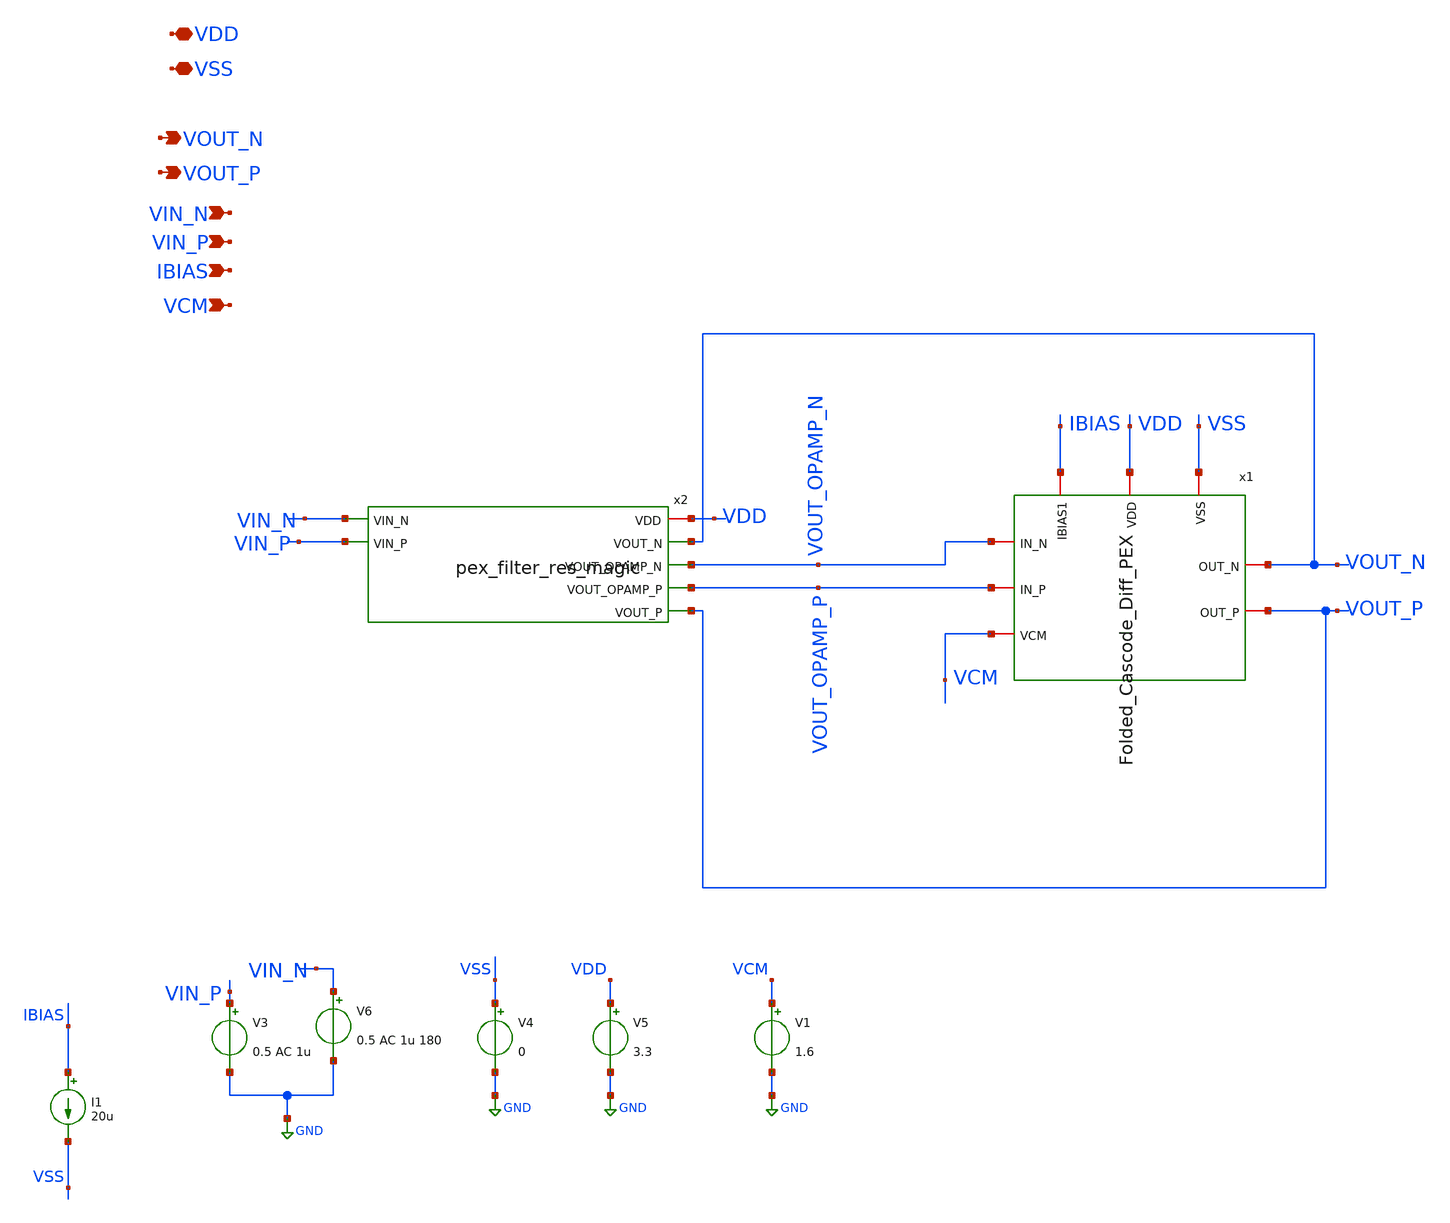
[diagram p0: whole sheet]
** sch_path: AWG_OUTPUT_AND_MUX_PAKISTAN_05/xschem/FILTER_OPAMPBLOCK_CHECK.sch
**.subckt FILTER_OPAMPBLOCK_CHECK VDD VSS VOUT_N VOUT_P VIN_N VIN_P IBIAS VCM
*.iopin VDD
*.iopin VSS
*.opin VOUT_N
*.opin VOUT_P
*.ipin VIN_N
*.ipin VIN_P
*.ipin IBIAS
*.ipin VCM
V3 VIN_P GND 0.5 AC 1u
V4 VSS GND 0
V5 VDD GND 3.3
V6 VIN_N GND 0.5 AC 1u 180
I1 IBIAS VSS 20u
V1 VCM GND 1.6
x2 VDD VOUT_N VOUT_OPAMP_N VOUT_OPAMP_P VOUT_P VIN_N VIN_P pex_filter_res_magic
x1 VDD VSS VOUT_OPAMP_N VOUT_OPAMP_P IBIAS VCM VOUT_N VOUT_P Folded_Cascode_Diff_PEX
**** begin user architecture code

.include $::180MCU_MODELS/design.ngspice
.lib $::180MCU_MODELS/sm141064.ngspice typical
.lib $::180MCU_MODELS/sm141064.ngspice res_typical
* .lib $::180MCU_MODELS/sm141064.ngspice res_statistical
.lib $::180MCU_MODELS/sm141064.ngspice mimcap_typical
.lib $::180MCU_MODELS/sm141064.ngspice cap_mim



.include pex_Folded_Diff_Op_Amp_Layout.spice
.include pex_filter_res_magic.spice
.control
set color0=white
set color1=black
save all

*.options savecurrents
save @m.x1.xm23.m0[vds] @m.x1.xm24.m0[vds]
*@m.xm4.m0[vds]
*save @m.xm8.m0[vds]
*save @m.xm10.m0[vds]
*save @m.xm12.m0[vds]
*-@m.xm1.m0[vdsat]
*dc V6 0 0.1 0.01m

*tran 150p 300n
*let gain = (maximum(outp)-minimum(outn))/2e-3
*print gain


*plot v(outp) v(outn)
*plot v(in1) v(in2)
*plot v(buff_in1) v(buff_in2)

ac dec 50 1 1e9
let tf = VOUT_N/VIN_P
let gain = db(tf)
let phase = (180/pi)*ph(tf)

*let tf1 = OUTp/IN1
*let gain1 = db(tf1)
*let phase1 = (180/pi)*ph(tf1)

plot gain
plot phase

*plot gain1
*plot phase1
*let myval=mean(out1)

*print myval
*let my_vect = [123 23 42 12 45 76]
*write pmos_nmos.raw
*let vdiff = @m.xm1.m0[vdsat]+vds
*plot @m.xm1.m0[vdsat]
*tran 100p 100n


*plot v(i1)
*plot vdiff
let m1vds = minimum(@m.x1.xm23.m0[vds])
let m2vds = minimum(@m.x1.xm24.m0[vds])
*let m4vds = minimum(@m.xm4.m0[vds])
*let m8vds = maximum(@m.xm8.m0[vds])
*let m10vds = maximum(@m.xm10.m0[vds])
*let m12vds = minimum(@m.xm12.m0[vds])
*print m1vds m2vds
*m4vds m8vds m10vds m12vds
*display all
.endc


**** end user architecture code
**.ends
.GLOBAL GND
.end
